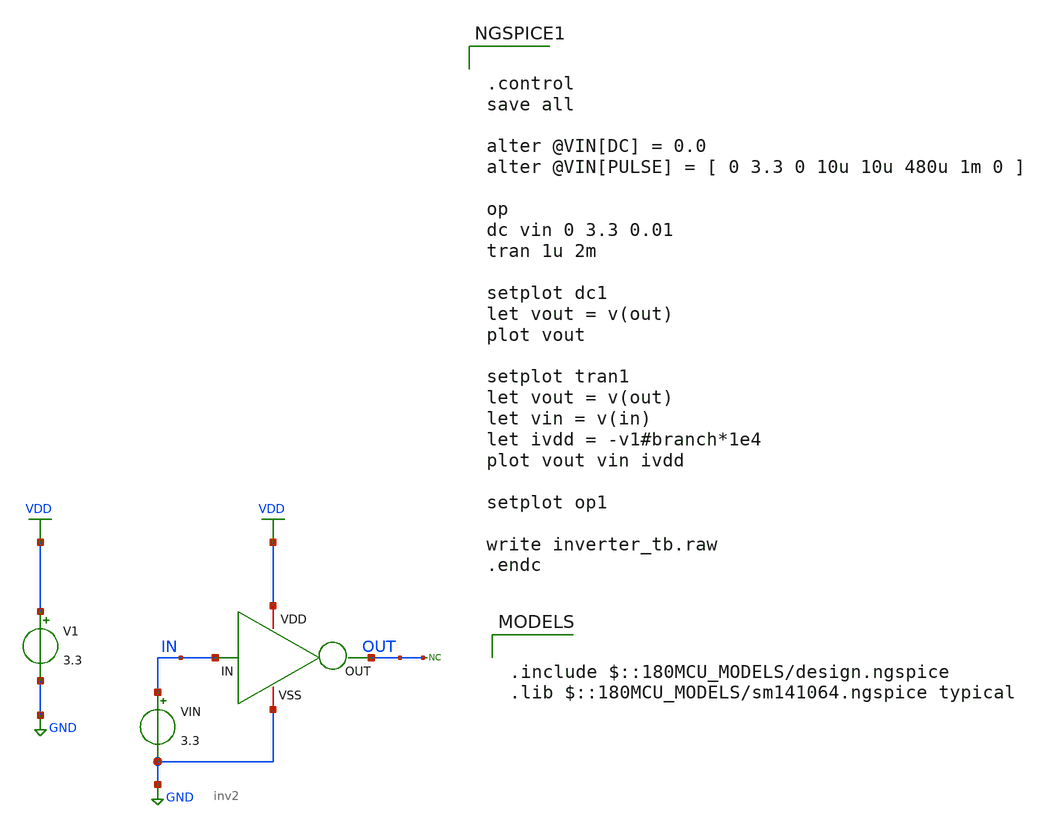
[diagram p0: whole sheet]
** sch_path: Array Components/Switch Array/CMOS Inverter/inv2_tb.sch
**.subckt inv2_tb
x1 VDD IN OUT GND inv2
V1 VDD GND 3.3
VIN IN GND 3.3
* noconn OUT
**** begin user architecture code

.include $::180MCU_MODELS/design.ngspice
.lib $::180MCU_MODELS/sm141064.ngspice typical



.control
save all

alter @VIN[DC] = 0.0
alter @VIN[PULSE] = [ 0 3.3 0 10u 10u 480u 1m 0 ]

op
dc vin 0 3.3 0.01
tran 1u 2m

setplot dc1
let vout = v(out)
plot vout

setplot tran1
let vout = v(out)
let vin = v(in)
let ivdd = -v1#branch*1e4
plot vout vin ivdd

setplot op1

write inverter_tb.raw
.endc


**** end user architecture code
**.ends

* expanding   symbol:  SAR ADC project/inv2.sym # of pins=4
** sym_path: Array Components/Switch Array/CMOS Inverter/inv2.sym
** sch_path: Array Components/Switch Array/CMOS Inverter/inv2.sch
.subckt inv2 VDD IN OUT VSS
*.iopin VDD
*.iopin VSS
*.ipin IN
*.opin OUT
XM1 OUT IN VSS VSS nfet_03v3 L=0.36u W=2u nf=1 ad='int((nf+1)/2) * W/nf * 0.18u' as='int((nf+2)/2) * W/nf * 0.18u'
+ pd='2*int((nf+1)/2) * (W/nf + 0.18u)' ps='2*int((nf+2)/2) * (W/nf + 0.18u)' nrd='0.18u / W' nrs='0.18u / W'
+ sa=0 sb=0 sd=0 m=1
XM2 OUT IN VDD VDD pfet_03v3 L=0.36u W=5u nf=1 ad='int((nf+1)/2) * W/nf * 0.18u' as='int((nf+2)/2) * W/nf * 0.18u'
+ pd='2*int((nf+1)/2) * (W/nf + 0.18u)' ps='2*int((nf+2)/2) * (W/nf + 0.18u)' nrd='0.18u / W' nrs='0.18u / W'
+ sa=0 sb=0 sd=0 m=1
.ends

.GLOBAL VDD
.GLOBAL GND
.end
